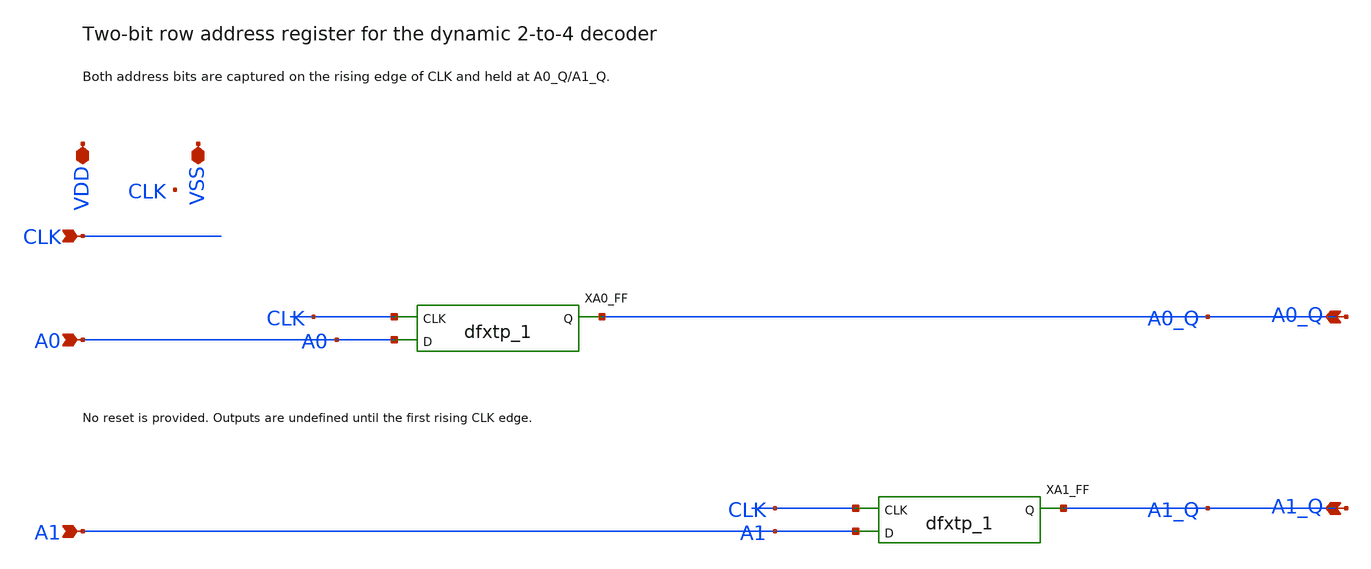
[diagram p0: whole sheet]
** sch_path: cells/control/row_address_capture.sch
**.subckt row_address_capture VDD VSS CLK A0 A1 A0_Q A1_Q
*.iopin VDD
*.iopin VSS
*.ipin CLK
*.ipin A0
*.ipin A1
*.opin A0_Q
*.opin A1_Q
XA0_FF CLK A0 VSS VSS VDD VDD A0_Q sky130_fd_sc_hd__dfxtp_1
XA1_FF CLK A1 VSS VSS VDD VDD A1_Q sky130_fd_sc_hd__dfxtp_1
**.ends
.end
